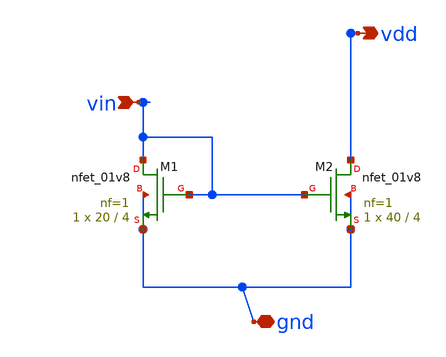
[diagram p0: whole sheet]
** sch_path: 05_layout/current_mirror.sch
**.subckt current_mirror vin vdd gnd
*.ipin vin
*.opin vdd
*.iopin gnd
XM1 vin vin gnd gnd sky130_fd_pr__nfet_01v8 L=4 W=20 nf=1 ad='int((1 + 1)/2) * 20 / 1 * 0.29' as='int((1 + 2)/2) * 20 / 1 * 0.29'
+ pd='2*int((1 + 1)/2) * (20 / 1 + 0.29)' ps='2*int((1 + 2)/2) * (20 / 1 + 0.29)' nrd='0.29 / 20 ' nrs='0.29 / 20 '
+ sa=0 sb=0 sd=0 mult=1 m=1
XM2 vdd vin gnd gnd sky130_fd_pr__nfet_01v8 L=4 W=40 nf=1 ad='int((1 + 1)/2) * 40 / 1 * 0.29' as='int((1 + 2)/2) * 40 / 1 * 0.29'
+ pd='2*int((1 + 1)/2) * (40 / 1 + 0.29)' ps='2*int((1 + 2)/2) * (40 / 1 + 0.29)' nrd='0.29 / 40 ' nrs='0.29 / 40 '
+ sa=0 sb=0 sd=0 mult=1 m=1
**.ends
.end
